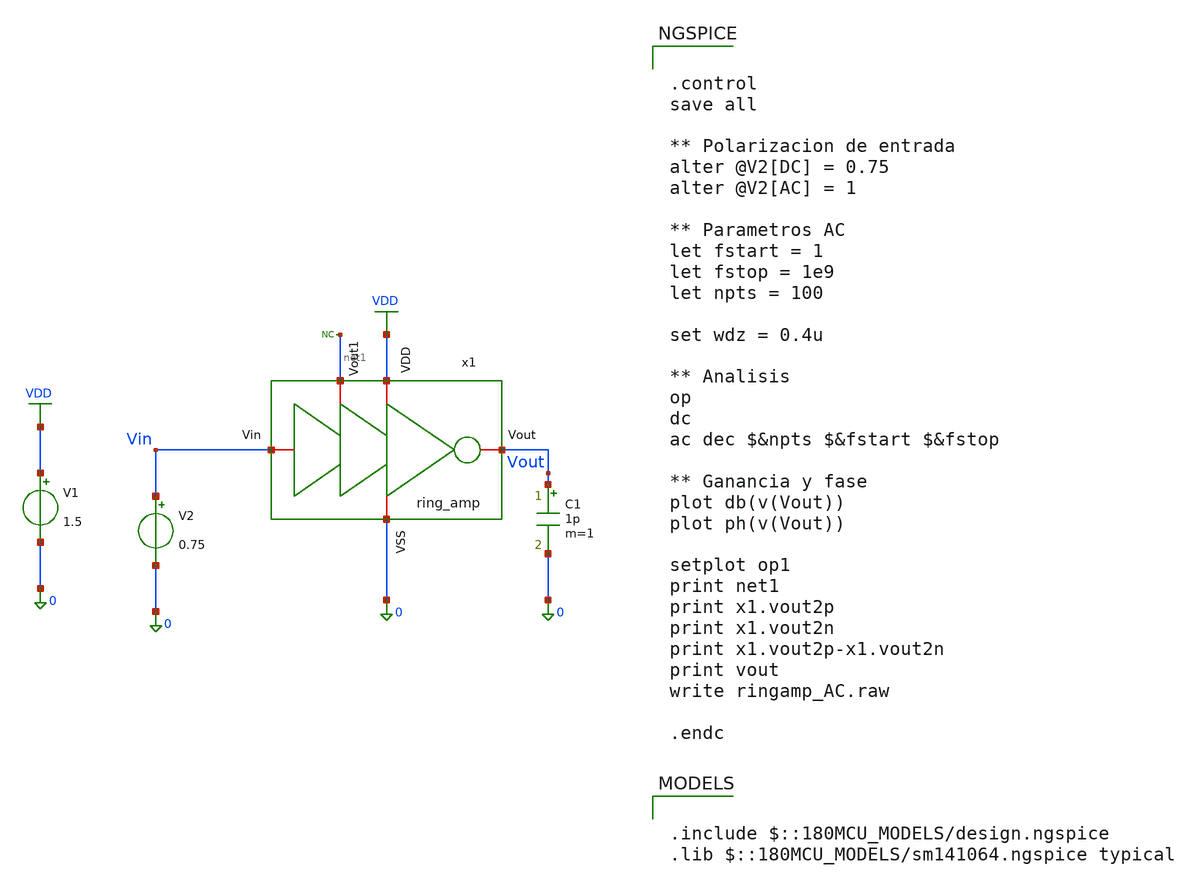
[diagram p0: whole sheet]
** sch_path: designs/DS_modulator/ring_amp/xschem/ring_amp_TB_AC.sch
**.subckt ring_amp_TB_AC
C1 Vout 0 1p m=1
* noconn #net1
V1 VDD 0 1.5
V2 Vin 0 0.75
x1 VDD Vin Vout net1 0 ring_amp
**** begin user architecture code

.include $::180MCU_MODELS/design.ngspice
.lib $::180MCU_MODELS/sm141064.ngspice typical



.control
save all

** Polarizacion de entrada
alter @V2[DC] = 0.75
alter @V2[AC] = 1

** Parametros AC
let fstart = 1
let fstop = 1e9
let npts = 100

set wdz = 0.4u

** Analisis
op
dc
ac dec $&npts $&fstart $&fstop

** Ganancia y fase
plot db(v(Vout))
plot ph(v(Vout))

setplot op1
print net1
print x1.vout2p
print x1.vout2n
print x1.vout2p-x1.vout2n
print vout
write ringamp_AC.raw

.endc


**** end user architecture code
**.ends
.GLOBAL VDD
.end
